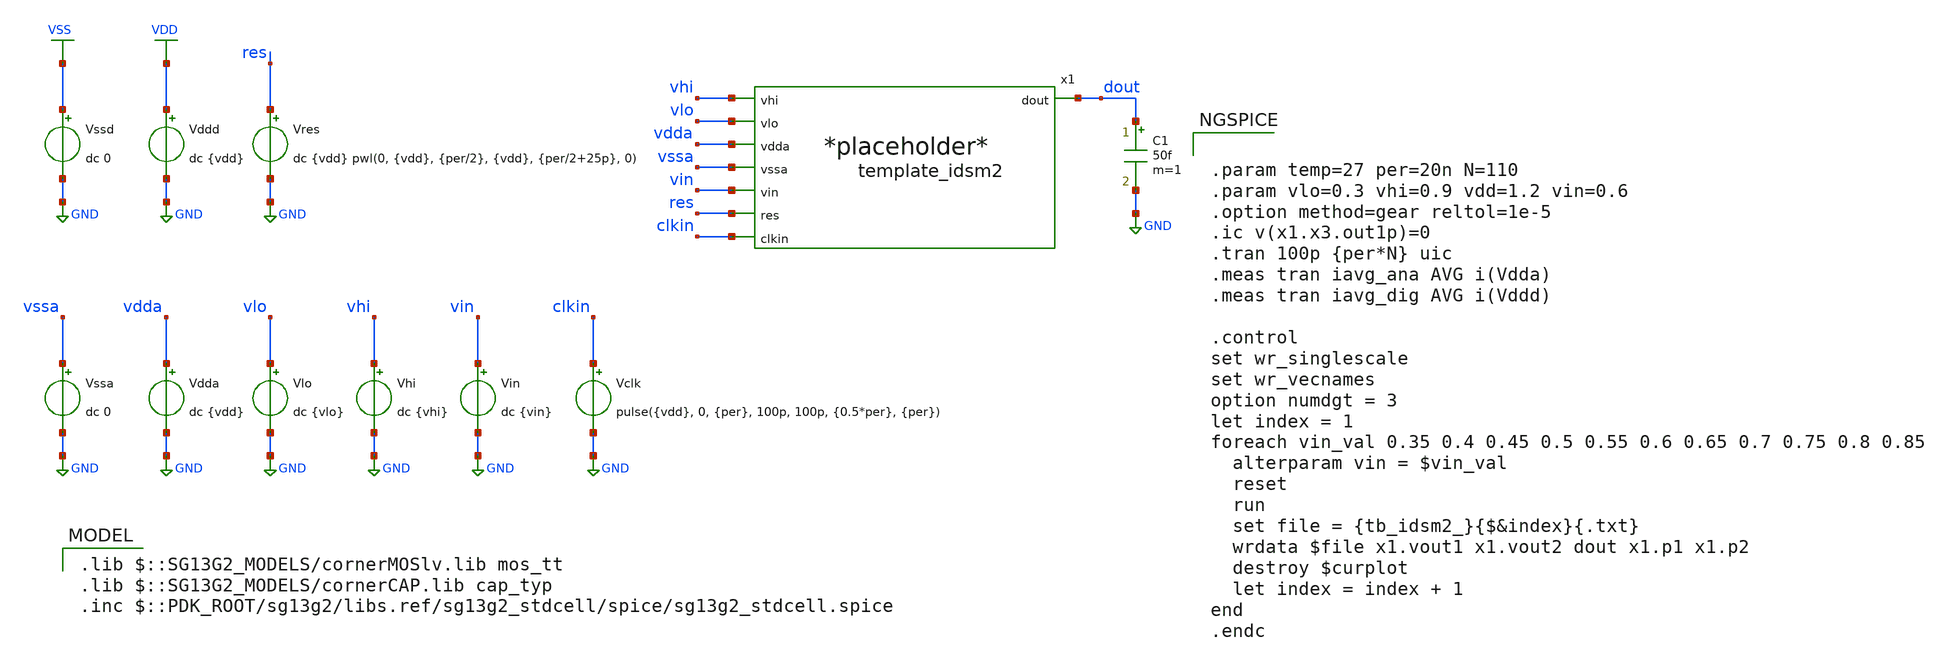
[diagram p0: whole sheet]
** sch_path: 5_Design/3_Real_circuits/tb_idsm2.sch
**.subckt tb_idsm2
Vin vin GND dc {vin}
Vssa vssa GND dc 0
Vres res GND dc {vdd} pwl(0, {vdd}, {per/2}, {vdd}, {per/2+25p}, 0)
Vclk clkin GND pulse({vdd}, 0, {per}, 100p, 100p, {0.5*per}, {per})
Vddd VDD GND dc {vdd}
Vssd VSS GND dc 0
Vdda vdda GND dc {vdd}
x1 vhi vlo vdda vssa vin dout res clkin template_idsm2
Vlo vlo GND dc {vlo}
Vhi vhi GND dc {vhi}
C1 dout GND 50f m=1
**** begin user architecture code


.param temp=27 per=20n N=110
.param vlo=0.3 vhi=0.9 vdd=1.2 vin=0.6
.option method=gear reltol=1e-5
.ic v(x1.x3.out1p)=0
.tran 100p {per*N} uic
.meas tran iavg_ana AVG i(Vdda)
.meas tran iavg_dig AVG i(Vddd)

.control
set wr_singlescale
set wr_vecnames
option numdgt = 3
let index = 1
foreach vin_val 0.35 0.4 0.45 0.5 0.55 0.6 0.65 0.7 0.75 0.8 0.85
  alterparam vin = $vin_val
  reset
  run
  set file = {tb_idsm2_}{$&index}{.txt}
  wrdata $file x1.vout1 x1.vout2 dout x1.p1 x1.p2
  destroy $curplot
  let index = index + 1
end
.endc


 .lib $::SG13G2_MODELS/cornerMOSlv.lib mos_tt
.lib $::SG13G2_MODELS/cornerCAP.lib cap_typ
.inc $::PDK_ROOT/sg13g2/libs.ref/sg13g2_stdcell/spice/sg13g2_stdcell.spice

**** end user architecture code
**.ends
.GLOBAL GND
.GLOBAL VDD
.GLOBAL VSS
.end
